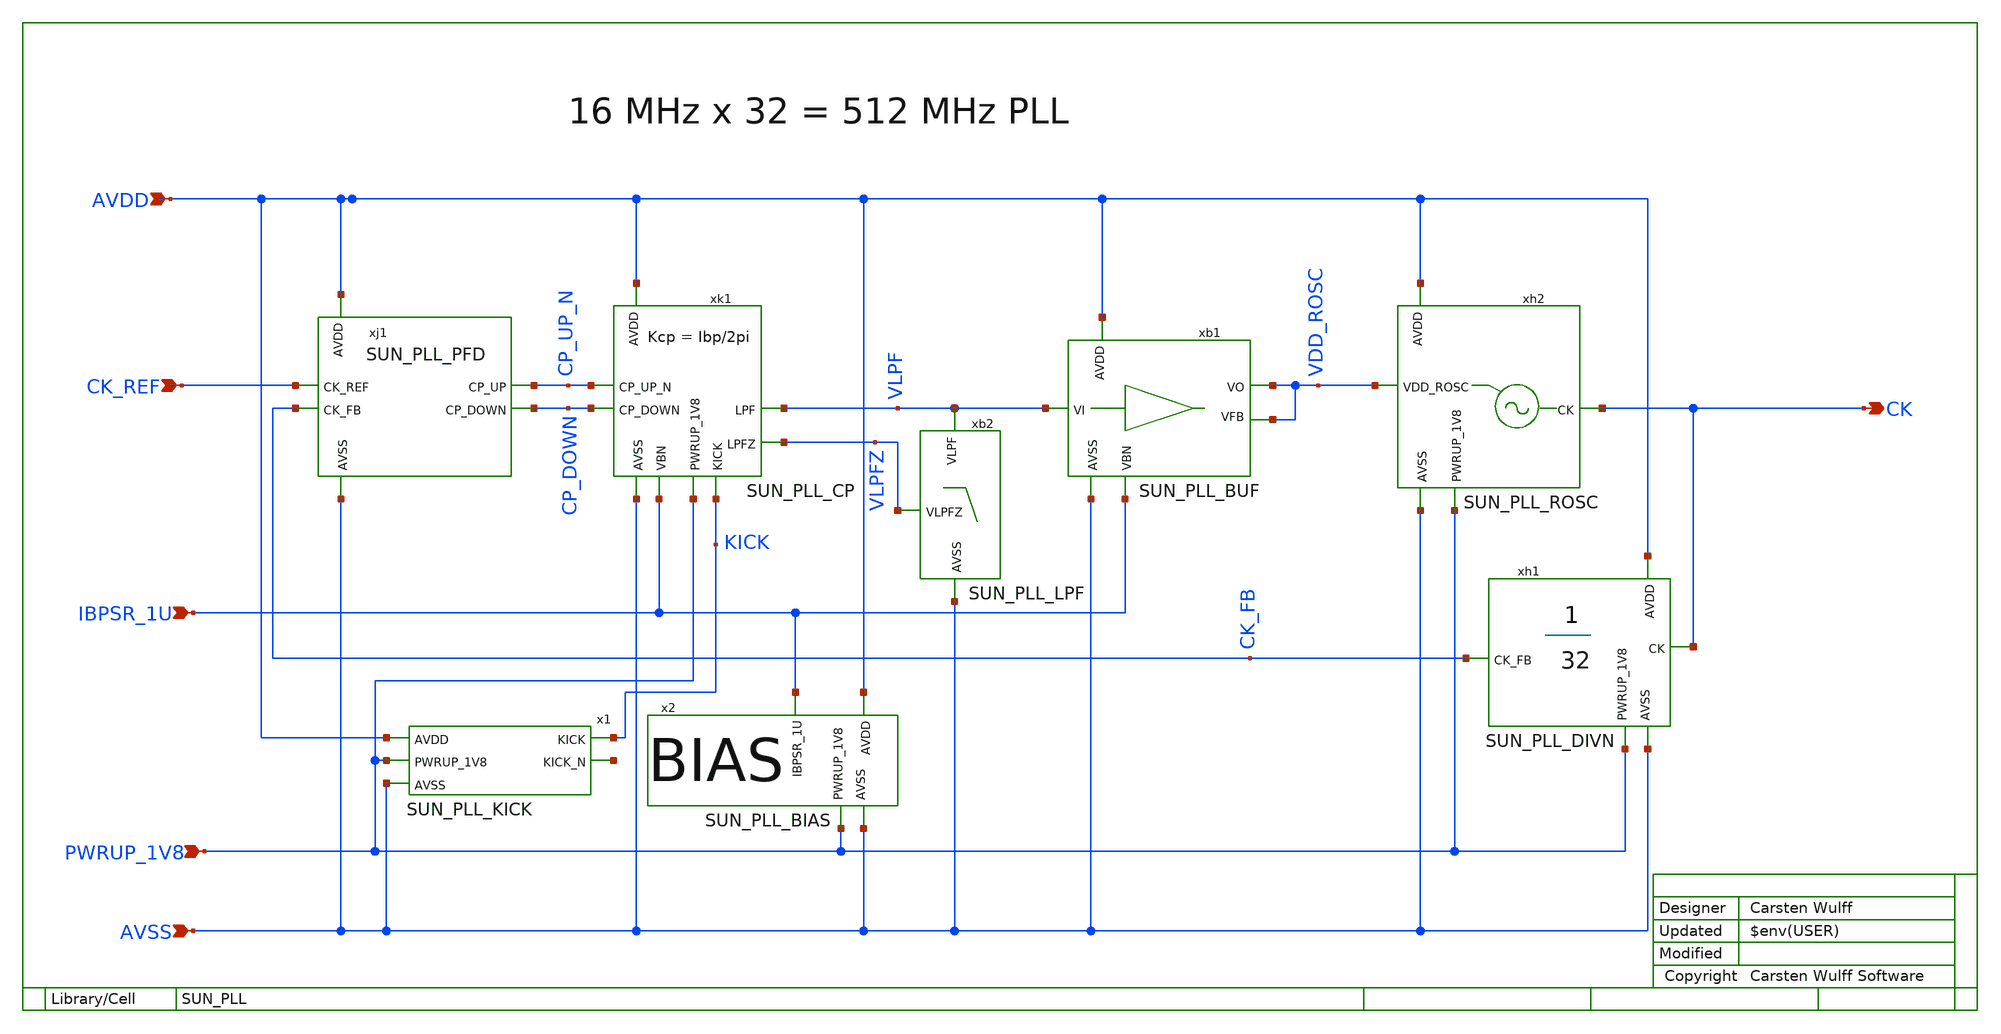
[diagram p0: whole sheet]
** sch_path: ip/sun_pll_sky130nm/design/SUN_PLL_SKY130NM/SUN_PLL.sch
**.subckt SUN_PLL AVDD AVSS PWRUP_1V8 CK_REF CK IBPSR_1U
*.ipin AVDD
*.ipin AVSS
*.ipin PWRUP_1V8
*.ipin CK_REF
*.opin CK
*.ipin IBPSR_1U
xh2 AVDD CK VDD_ROSC PWRUP_1V8 AVSS SUN_PLL_ROSC xoffset=0 yoffset=0 angle=0
xh1 AVDD CK_FB CK PWRUP_1V8 AVSS SUN_PLL_DIVN xoffset=-300 yoffset=12 angle=0
x2 IBPSR_1U AVDD PWRUP_1V8 AVSS SUN_PLL_BIAS xoffset=0 yoffset=10 angle=0
xb1 AVDD VDD_ROSC VLPF VDD_ROSC IBPSR_1U AVSS SUN_PLL_BUF xoffset=5 yoffset=2 angle=0
xb2 VLPFZ AVSS VLPF SUN_PLL_LPF xoffset=0 yoffset=40 angle=0
xk1 AVDD CP_UP_N VLPF CP_DOWN IBPSR_1U AVSS VLPFZ PWRUP_1V8 KICK SUN_PLL_CP xoffset=60 yoffset=4
+ angle=0
xj1 AVDD CP_UP_N CK_REF CP_DOWN CK_FB AVSS SUN_PLL_PFD
x1 AVDD KICK net1 PWRUP_1V8 AVSS SUN_PLL_KICK
**.ends
.end
